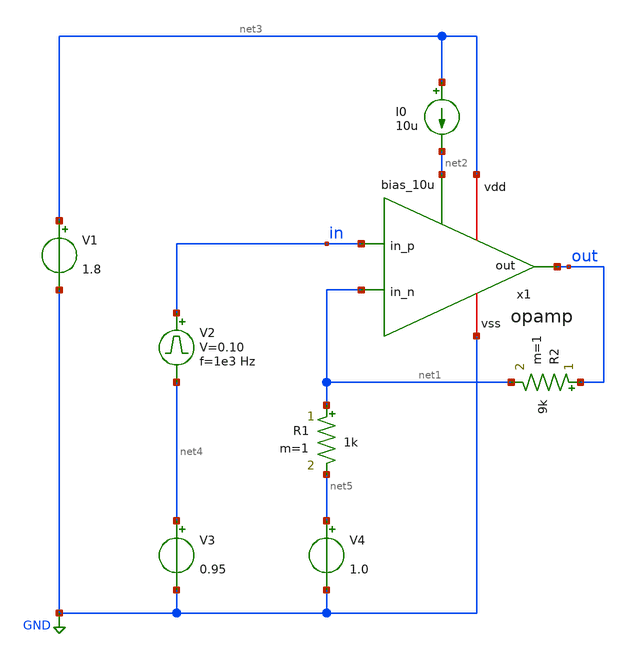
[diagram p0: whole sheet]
** sch_path: design/opamp/test/test_opamp_tran.sch
**.subckt test_opamp_tran
x1 net3 net1 in out net2 GND opamp
I0 net3 net2 10u
V1 net3 GND 1.8
R1 net1 net5 1k m=1
R2 out net1 9k m=1
V2 in net4 pulse 0 0.10 '0.495/ 1e3 ' '0.01/1e3 ' '0.01/1e3 ' '0.49/1e3 ' '1/1e3 '
V3 net4 GND 0.95
V4 net5 GND 1.0
**** begin user architecture code


.param temp=27

*.op
*.ac dec 10 1 10G

.control
tran 1u 10m
plot v(out)
.endc

.save all




.options wnflag=1
.include $::SKYWATER_MODELS/cells/nfet_01v8/sky130_fd_pr__nfet_01v8__tt.corner.spice
.include $::SKYWATER_MODELS/cells/nfet_01v8_lvt/sky130_fd_pr__nfet_01v8_lvt__tt.corner.spice
.include $::SKYWATER_MODELS/cells/pfet_01v8/sky130_fd_pr__pfet_01v8__tt.corner.spice
.include $::SKYWATER_MODELS/cells/nfet_03v3_nvt/sky130_fd_pr__nfet_03v3_nvt__tt.corner.spice
.include $::SKYWATER_MODELS/cells/nfet_05v0_nvt/sky130_fd_pr__nfet_05v0_nvt__tt.corner.spice
.include $::SKYWATER_MODELS/cells/esd_nfet_01v8/sky130_fd_pr__esd_nfet_01v8__tt.corner.spice
.include $::SKYWATER_MODELS/cells/pfet_01v8_lvt/sky130_fd_pr__pfet_01v8_lvt__tt.corner.spice
.include $::SKYWATER_MODELS/cells/pfet_01v8_hvt/sky130_fd_pr__pfet_01v8_hvt__tt.corner.spice
.include $::SKYWATER_MODELS/cells/esd_pfet_g5v0d10v5/sky130_fd_pr__esd_pfet_g5v0d10v5__tt.corner.spice
.include $::SKYWATER_MODELS/cells/pfet_g5v0d10v5/sky130_fd_pr__pfet_g5v0d10v5__tt.corner.spice
.include $::SKYWATER_MODELS/cells/pfet_g5v0d16v0/sky130_fd_pr__pfet_g5v0d16v0__tt.corner.spice
.include $::SKYWATER_MODELS/cells/nfet_g5v0d10v5/sky130_fd_pr__nfet_g5v0d10v5__tt.corner.spice
.include $::SKYWATER_MODELS/cells/nfet_g5v0d16v0/sky130_fd_pr__nfet_g5v0d16v0__tt_discrete.corner.spice
.include $::SKYWATER_MODELS/cells/esd_nfet_g5v0d10v5/sky130_fd_pr__esd_nfet_g5v0d10v5__tt.corner.spice
.include $::SKYWATER_MODELS/models/corners/tt/nonfet.spice
* Mismatch parameters
.include $::SKYWATER_MODELS/cells/nfet_01v8/sky130_fd_pr__nfet_01v8__mismatch.corner.spice
.include $::SKYWATER_MODELS/cells/pfet_01v8/sky130_fd_pr__pfet_01v8__mismatch.corner.spice
.include $::SKYWATER_MODELS/cells/nfet_01v8_lvt/sky130_fd_pr__nfet_01v8_lvt__mismatch.corner.spice
.include $::SKYWATER_MODELS/cells/pfet_01v8_lvt/sky130_fd_pr__pfet_01v8_lvt__mismatch.corner.spice
.include $::SKYWATER_MODELS/cells/pfet_01v8_hvt/sky130_fd_pr__pfet_01v8_hvt__mismatch.corner.spice
.include $::SKYWATER_MODELS/cells/nfet_g5v0d10v5/sky130_fd_pr__nfet_g5v0d10v5__mismatch.corner.spice
.include $::SKYWATER_MODELS/cells/pfet_g5v0d10v5/sky130_fd_pr__pfet_g5v0d10v5__mismatch.corner.spice
.include $::SKYWATER_MODELS/cells/nfet_05v0_nvt/sky130_fd_pr__nfet_05v0_nvt__mismatch.corner.spice
.include $::SKYWATER_MODELS/cells/nfet_03v3_nvt/sky130_fd_pr__nfet_03v3_nvt__mismatch.corner.spice
* Resistor$::SKYWATER_MODELS/Capacitor
.include $::SKYWATER_MODELS/models/r+c/res_typical__cap_typical.spice
.include $::SKYWATER_MODELS/models/r+c/res_typical__cap_typical__lin.spice
* Special cells
.include $::SKYWATER_MODELS/models/corners/tt/specialized_cells.spice
* All models
.include $::SKYWATER_MODELS/models/all.spice
* Corner
.include $::SKYWATER_MODELS/models/corners/tt/rf.spice

**** end user architecture code
**.ends

* expanding   symbol:  opamp/opamp.sym # of pins=6
** sym_path: design/opamp/opamp.sym
** sch_path: design/opamp/opamp.sch
.subckt opamp vdd in_n in_p out bias_10u vss
*.iopin vdd
*.iopin vss
*.ipin in_n
*.ipin in_p
*.opin out
*.ipin bias_10u
XM1 bias_10u bias_10u vss vss sky130_fd_pr__nfet_01v8_lvt L=2 W=1 nf=1 ad='int((nf+1)/2) * W/nf * 0.29'
+ as='int((nf+2)/2) * W/nf * 0.29' pd='2*int((nf+1)/2) * (W/nf + 0.29)' ps='2*int((nf+2)/2) * (W/nf + 0.29)'
+ nrd='0.29 / W' nrs='0.29 / W' sa=0 sb=0 sd=0 mult=1 m=1
XM2 net2 in_n net1 vss sky130_fd_pr__nfet_01v8_lvt L=0.25 W=10 nf=1 ad='int((nf+1)/2) * W/nf * 0.29'
+ as='int((nf+2)/2) * W/nf * 0.29' pd='2*int((nf+1)/2) * (W/nf + 0.29)' ps='2*int((nf+2)/2) * (W/nf + 0.29)'
+ nrd='0.29 / W' nrs='0.29 / W' sa=0 sb=0 sd=0 mult=10 m=10
XM3 net3 in_p net1 vss sky130_fd_pr__nfet_01v8_lvt L=0.25 W=10 nf=1 ad='int((nf+1)/2) * W/nf * 0.29'
+ as='int((nf+2)/2) * W/nf * 0.29' pd='2*int((nf+1)/2) * (W/nf + 0.29)' ps='2*int((nf+2)/2) * (W/nf + 0.29)'
+ nrd='0.29 / W' nrs='0.29 / W' sa=0 sb=0 sd=0 mult=10 m=10
XM4 net1 bias_10u vss vss sky130_fd_pr__nfet_01v8_lvt L=2 W=1 nf=1 ad='int((nf+1)/2) * W/nf * 0.29' as='int((nf+2)/2) * W/nf * 0.29'
+ pd='2*int((nf+1)/2) * (W/nf + 0.29)' ps='2*int((nf+2)/2) * (W/nf + 0.29)' nrd='0.29 / W' nrs='0.29 / W'
+ sa=0 sb=0 sd=0 mult=2 m=2
XM5 out bias_10u vss vss sky130_fd_pr__nfet_01v8_lvt L=2 W=1 nf=1 ad='int((nf+1)/2) * W/nf * 0.29' as='int((nf+2)/2) * W/nf * 0.29'
+ pd='2*int((nf+1)/2) * (W/nf + 0.29)' ps='2*int((nf+2)/2) * (W/nf + 0.29)' nrd='0.29 / W' nrs='0.29 / W'
+ sa=0 sb=0 sd=0 mult=10 m=10
XM6 net3 net2 vdd vdd sky130_fd_pr__pfet_01v8_lvt L=0.5 W=1 nf=1 ad='int((nf+1)/2) * W/nf * 0.29' as='int((nf+2)/2) * W/nf * 0.29'
+ pd='2*int((nf+1)/2) * (W/nf + 0.29)' ps='2*int((nf+2)/2) * (W/nf + 0.29)' nrd='0.29 / W' nrs='0.29 / W'
+ sa=0 sb=0 sd=0 mult=1 m=1
XM7 net2 net2 vdd vdd sky130_fd_pr__pfet_01v8_lvt L=0.5 W=1 nf=1 ad='int((nf+1)/2) * W/nf * 0.29' as='int((nf+2)/2) * W/nf * 0.29'
+ pd='2*int((nf+1)/2) * (W/nf + 0.29)' ps='2*int((nf+2)/2) * (W/nf + 0.29)' nrd='0.29 / W' nrs='0.29 / W'
+ sa=0 sb=0 sd=0 mult=1 m=1
XM8 out net3 vdd vdd sky130_fd_pr__pfet_01v8_lvt L=0.5 W=1 nf=1 ad='int((nf+1)/2) * W/nf * 0.29' as='int((nf+2)/2) * W/nf * 0.29'
+ pd='2*int((nf+1)/2) * (W/nf + 0.29)' ps='2*int((nf+2)/2) * (W/nf + 0.29)' nrd='0.29 / W' nrs='0.29 / W'
+ sa=0 sb=0 sd=0 mult=10 m=10
.ends

.GLOBAL GND
.end
